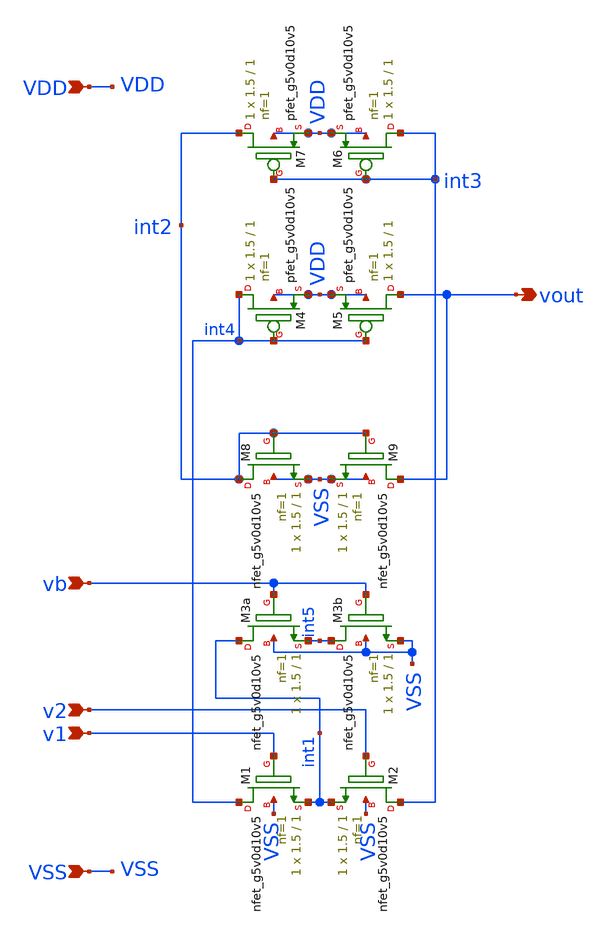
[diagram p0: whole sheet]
** sch_path: xschem/diffamp_nmos.sch
**.subckt diffamp_nmos v1 v2 vb vout VDD VSS
*.ipin v1
*.ipin v2
*.ipin vb
*.opin vout
*.ipin VDD
*.ipin VSS
XM7 int2 int3 VDD VDD sky130_fd_pr__pfet_g5v0d10v5 L=1 W=1.5 nf=1 ad='int((nf+1)/2) * W/nf * 0.29' as='int((nf+2)/2) * W/nf * 0.29'
+ pd='2*int((nf+1)/2) * (W/nf + 0.29)' ps='2*int((nf+2)/2) * (W/nf + 0.29)' nrd='0.29 / W' nrs='0.29 / W'
+ sa=0 sb=0 sd=0 mult=1 m=1
XM8 int2 int2 VSS VSS sky130_fd_pr__nfet_g5v0d10v5 L=1 W=1.5 nf=1 ad='int((nf+1)/2) * W/nf * 0.29' as='int((nf+2)/2) * W/nf * 0.29'
+ pd='2*int((nf+1)/2) * (W/nf + 0.29)' ps='2*int((nf+2)/2) * (W/nf + 0.29)' nrd='0.29 / W' nrs='0.29 / W'
+ sa=0 sb=0 sd=0 mult=1 m=1
XM9 vout int2 VSS VSS sky130_fd_pr__nfet_g5v0d10v5 L=1 W=1.5 nf=1 ad='int((nf+1)/2) * W/nf * 0.29' as='int((nf+2)/2) * W/nf * 0.29'
+ pd='2*int((nf+1)/2) * (W/nf + 0.29)' ps='2*int((nf+2)/2) * (W/nf + 0.29)' nrd='0.29 / W' nrs='0.29 / W'
+ sa=0 sb=0 sd=0 mult=1 m=1
XM1 int4 v1 int1 VSS sky130_fd_pr__nfet_g5v0d10v5 L=1 W=1.5 nf=1 ad='int((nf+1)/2) * W/nf * 0.29' as='int((nf+2)/2) * W/nf * 0.29'
+ pd='2*int((nf+1)/2) * (W/nf + 0.29)' ps='2*int((nf+2)/2) * (W/nf + 0.29)' nrd='0.29 / W' nrs='0.29 / W'
+ sa=0 sb=0 sd=0 mult=1 m=1
XM2 int3 v2 int1 VSS sky130_fd_pr__nfet_g5v0d10v5 L=1 W=1.5 nf=1 ad='int((nf+1)/2) * W/nf * 0.29' as='int((nf+2)/2) * W/nf * 0.29'
+ pd='2*int((nf+1)/2) * (W/nf + 0.29)' ps='2*int((nf+2)/2) * (W/nf + 0.29)' nrd='0.29 / W' nrs='0.29 / W'
+ sa=0 sb=0 sd=0 mult=1 m=1
XM6 int3 int3 VDD VDD sky130_fd_pr__pfet_g5v0d10v5 L=1 W=1.5 nf=1 ad='int((nf+1)/2) * W/nf * 0.29' as='int((nf+2)/2) * W/nf * 0.29'
+ pd='2*int((nf+1)/2) * (W/nf + 0.29)' ps='2*int((nf+2)/2) * (W/nf + 0.29)' nrd='0.29 / W' nrs='0.29 / W'
+ sa=0 sb=0 sd=0 mult=1 m=1
XM5 vout int4 VDD VDD sky130_fd_pr__pfet_g5v0d10v5 L=1 W=1.5 nf=1 ad='int((nf+1)/2) * W/nf * 0.29' as='int((nf+2)/2) * W/nf * 0.29'
+ pd='2*int((nf+1)/2) * (W/nf + 0.29)' ps='2*int((nf+2)/2) * (W/nf + 0.29)' nrd='0.29 / W' nrs='0.29 / W'
+ sa=0 sb=0 sd=0 mult=1 m=1
XM3a int1 vb int5 VSS sky130_fd_pr__nfet_g5v0d10v5 L=1 W=1.5 nf=1 ad='int((nf+1)/2) * W/nf * 0.29' as='int((nf+2)/2) * W/nf * 0.29'
+ pd='2*int((nf+1)/2) * (W/nf + 0.29)' ps='2*int((nf+2)/2) * (W/nf + 0.29)' nrd='0.29 / W' nrs='0.29 / W'
+ sa=0 sb=0 sd=0 mult=1 m=1
XM3b int5 vb VSS VSS sky130_fd_pr__nfet_g5v0d10v5 L=1 W=1.5 nf=1 ad='int((nf+1)/2) * W/nf * 0.29' as='int((nf+2)/2) * W/nf * 0.29'
+ pd='2*int((nf+1)/2) * (W/nf + 0.29)' ps='2*int((nf+2)/2) * (W/nf + 0.29)' nrd='0.29 / W' nrs='0.29 / W'
+ sa=0 sb=0 sd=0 mult=1 m=1
XM4 int4 int4 VDD VDD sky130_fd_pr__pfet_g5v0d10v5 L=1 W=1.5 nf=1 ad='int((nf+1)/2) * W/nf * 0.29' as='int((nf+2)/2) * W/nf * 0.29'
+ pd='2*int((nf+1)/2) * (W/nf + 0.29)' ps='2*int((nf+2)/2) * (W/nf + 0.29)' nrd='0.29 / W' nrs='0.29 / W'
+ sa=0 sb=0 sd=0 mult=1 m=1
**.ends
.end
